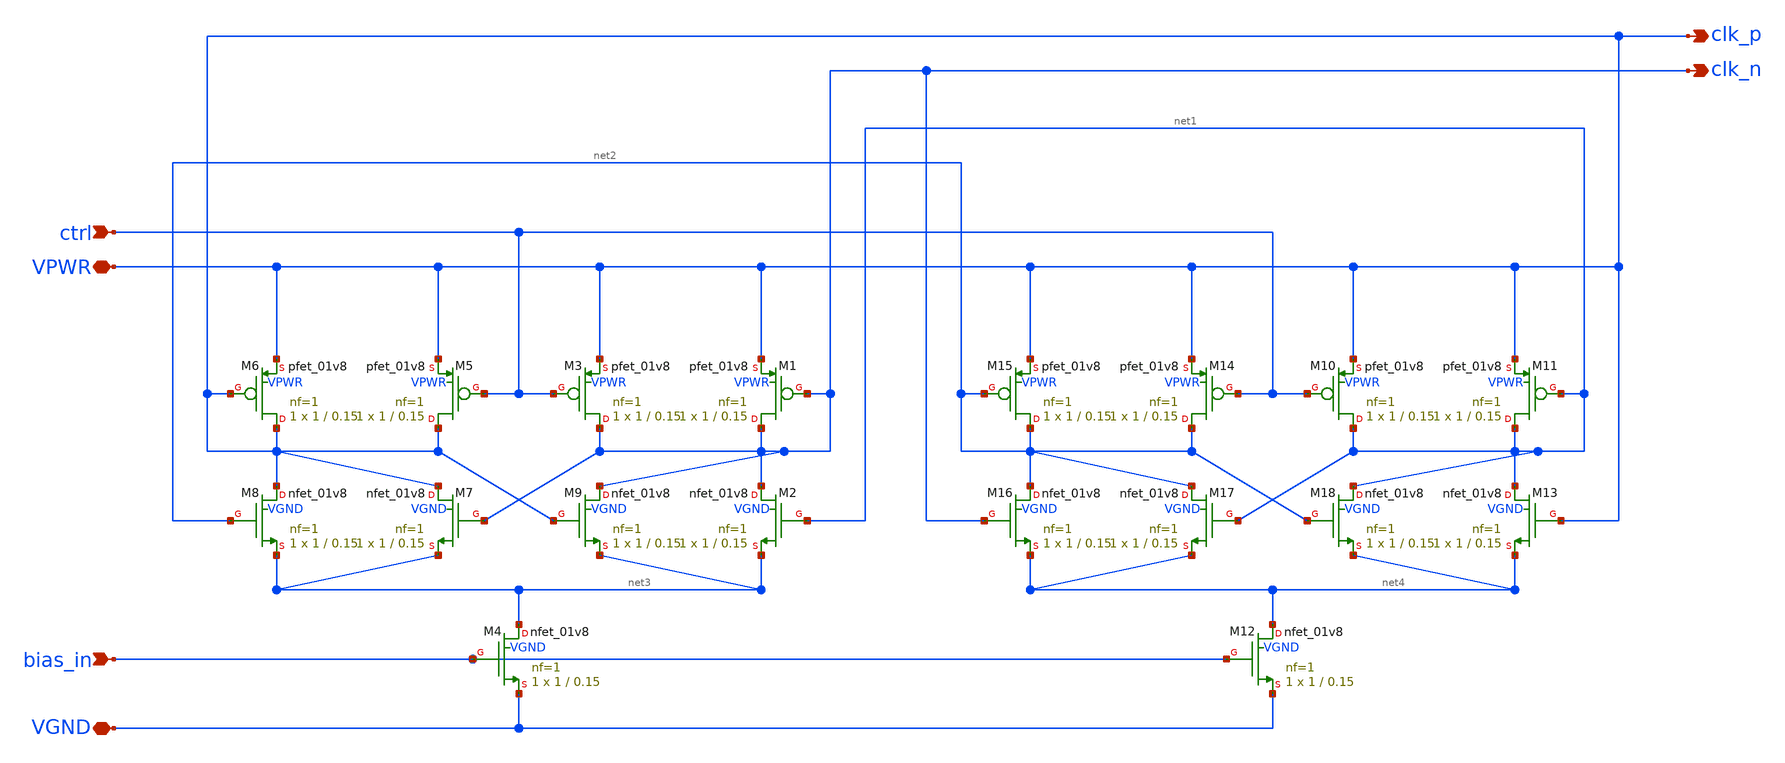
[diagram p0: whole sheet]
** sch_path: simple_vco/v1/clk_core.sch
**.subckt clk_core VPWR VGND ctrl bias_in clk_p clk_n
*.iopin VPWR
*.iopin VGND
*.ipin ctrl
*.ipin bias_in
*.opin clk_p
*.opin clk_n
XM3 clk_n ctrl VPWR VPWR sky130_fd_pr__pfet_01v8 L=0.15 W=1 nf=1 ad='int((1 + 1)/2) * 1 / 1 * 0.29' as='int((1 + 2)/2) * 1 / 1 * 0.29'
+ pd='2*int((1 + 1)/2) * (1 / 1 + 0.29)' ps='2*int((1 + 2)/2) * (1 / 1 + 0.29)' nrd='0.29 / 1 ' nrs='0.29 / 1 '
+ sa=0 sb=0 sd=0 mult=1 m=1
XM1 clk_n clk_n VPWR VPWR sky130_fd_pr__pfet_01v8 L=0.15 W=1 nf=1 ad='int((1 + 1)/2) * 1 / 1 * 0.29'
+ as='int((1 + 2)/2) * 1 / 1 * 0.29' pd='2*int((1 + 1)/2) * (1 / 1 + 0.29)' ps='2*int((1 + 2)/2) * (1 / 1 + 0.29)'
+ nrd='0.29 / 1 ' nrs='0.29 / 1 ' sa=0 sb=0 sd=0 mult=1 m=1
XM4 net3 bias_in VGND VGND sky130_fd_pr__nfet_01v8 L=0.15 W=1 nf=1 ad='int((1 + 1)/2) * 1 / 1 * 0.29'
+ as='int((1 + 2)/2) * 1 / 1 * 0.29' pd='2*int((1 + 1)/2) * (1 / 1 + 0.29)' ps='2*int((1 + 2)/2) * (1 / 1 + 0.29)'
+ nrd='0.29 / 1 ' nrs='0.29 / 1 ' sa=0 sb=0 sd=0 mult=1 m=1
XM2 clk_n net1 net3 VGND sky130_fd_pr__nfet_01v8 L=0.15 W=1 nf=1 ad='int((1 + 1)/2) * 1 / 1 * 0.29' as='int((1 + 2)/2) * 1 / 1 * 0.29'
+ pd='2*int((1 + 1)/2) * (1 / 1 + 0.29)' ps='2*int((1 + 2)/2) * (1 / 1 + 0.29)' nrd='0.29 / 1 ' nrs='0.29 / 1 '
+ sa=0 sb=0 sd=0 mult=1 m=1
XM5 VPWR ctrl VPWR VPWR sky130_fd_pr__pfet_01v8 L=0.15 W=1 nf=1 ad='int((1 + 1)/2) * 1 / 1 * 0.29' as='int((1 + 2)/2) * 1 / 1 * 0.29'
+ pd='2*int((1 + 1)/2) * (1 / 1 + 0.29)' ps='2*int((1 + 2)/2) * (1 / 1 + 0.29)' nrd='0.29 / 1 ' nrs='0.29 / 1 '
+ sa=0 sb=0 sd=0 mult=1 m=1
XM6 VPWR VPWR VPWR VPWR sky130_fd_pr__pfet_01v8 L=0.15 W=1 nf=1 ad='int((1 + 1)/2) * 1 / 1 * 0.29' as='int((1 + 2)/2) * 1 / 1 * 0.29'
+ pd='2*int((1 + 1)/2) * (1 / 1 + 0.29)' ps='2*int((1 + 2)/2) * (1 / 1 + 0.29)' nrd='0.29 / 1 ' nrs='0.29 / 1 '
+ sa=0 sb=0 sd=0 mult=1 m=1
XM8 VPWR net2 net3 VGND sky130_fd_pr__nfet_01v8 L=0.15 W=1 nf=1 ad='int((1 + 1)/2) * 1 / 1 * 0.29' as='int((1 + 2)/2) * 1 / 1 * 0.29'
+ pd='2*int((1 + 1)/2) * (1 / 1 + 0.29)' ps='2*int((1 + 2)/2) * (1 / 1 + 0.29)' nrd='0.29 / 1 ' nrs='0.29 / 1 '
+ sa=0 sb=0 sd=0 mult=1 m=1
XM7 VPWR clk_n net3 VGND sky130_fd_pr__nfet_01v8 L=0.15 W=1 nf=1 ad='int((1 + 1)/2) * 1 / 1 * 0.29' as='int((1 + 2)/2) * 1 / 1 * 0.29'
+ pd='2*int((1 + 1)/2) * (1 / 1 + 0.29)' ps='2*int((1 + 2)/2) * (1 / 1 + 0.29)' nrd='0.29 / 1 ' nrs='0.29 / 1 '
+ sa=0 sb=0 sd=0 mult=1 m=1
XM9 clk_n VPWR net3 VGND sky130_fd_pr__nfet_01v8 L=0.15 W=1 nf=1 ad='int((1 + 1)/2) * 1 / 1 * 0.29' as='int((1 + 2)/2) * 1 / 1 * 0.29'
+ pd='2*int((1 + 1)/2) * (1 / 1 + 0.29)' ps='2*int((1 + 2)/2) * (1 / 1 + 0.29)' nrd='0.29 / 1 ' nrs='0.29 / 1 '
+ sa=0 sb=0 sd=0 mult=1 m=1
XM10 net1 ctrl VPWR VPWR sky130_fd_pr__pfet_01v8 L=0.15 W=1 nf=1 ad='int((1 + 1)/2) * 1 / 1 * 0.29' as='int((1 + 2)/2) * 1 / 1 * 0.29'
+ pd='2*int((1 + 1)/2) * (1 / 1 + 0.29)' ps='2*int((1 + 2)/2) * (1 / 1 + 0.29)' nrd='0.29 / 1 ' nrs='0.29 / 1 '
+ sa=0 sb=0 sd=0 mult=1 m=1
XM11 net1 net1 VPWR VPWR sky130_fd_pr__pfet_01v8 L=0.15 W=1 nf=1 ad='int((1 + 1)/2) * 1 / 1 * 0.29' as='int((1 + 2)/2) * 1 / 1 * 0.29'
+ pd='2*int((1 + 1)/2) * (1 / 1 + 0.29)' ps='2*int((1 + 2)/2) * (1 / 1 + 0.29)' nrd='0.29 / 1 ' nrs='0.29 / 1 '
+ sa=0 sb=0 sd=0 mult=1 m=1
XM12 net4 bias_in VGND VGND sky130_fd_pr__nfet_01v8 L=0.15 W=1 nf=1 ad='int((1 + 1)/2) * 1 / 1 * 0.29'
+ as='int((1 + 2)/2) * 1 / 1 * 0.29' pd='2*int((1 + 1)/2) * (1 / 1 + 0.29)' ps='2*int((1 + 2)/2) * (1 / 1 + 0.29)'
+ nrd='0.29 / 1 ' nrs='0.29 / 1 ' sa=0 sb=0 sd=0 mult=1 m=1
XM13 net1 VPWR net4 VGND sky130_fd_pr__nfet_01v8 L=0.15 W=1 nf=1 ad='int((1 + 1)/2) * 1 / 1 * 0.29' as='int((1 + 2)/2) * 1 / 1 * 0.29'
+ pd='2*int((1 + 1)/2) * (1 / 1 + 0.29)' ps='2*int((1 + 2)/2) * (1 / 1 + 0.29)' nrd='0.29 / 1 ' nrs='0.29 / 1 '
+ sa=0 sb=0 sd=0 mult=1 m=1
XM14 net2 ctrl VPWR VPWR sky130_fd_pr__pfet_01v8 L=0.15 W=1 nf=1 ad='int((1 + 1)/2) * 1 / 1 * 0.29' as='int((1 + 2)/2) * 1 / 1 * 0.29'
+ pd='2*int((1 + 1)/2) * (1 / 1 + 0.29)' ps='2*int((1 + 2)/2) * (1 / 1 + 0.29)' nrd='0.29 / 1 ' nrs='0.29 / 1 '
+ sa=0 sb=0 sd=0 mult=1 m=1
XM15 net2 net2 VPWR VPWR sky130_fd_pr__pfet_01v8 L=0.15 W=1 nf=1 ad='int((1 + 1)/2) * 1 / 1 * 0.29' as='int((1 + 2)/2) * 1 / 1 * 0.29'
+ pd='2*int((1 + 1)/2) * (1 / 1 + 0.29)' ps='2*int((1 + 2)/2) * (1 / 1 + 0.29)' nrd='0.29 / 1 ' nrs='0.29 / 1 '
+ sa=0 sb=0 sd=0 mult=1 m=1
XM16 net2 clk_n net4 VGND sky130_fd_pr__nfet_01v8 L=0.15 W=1 nf=1 ad='int((1 + 1)/2) * 1 / 1 * 0.29'
+ as='int((1 + 2)/2) * 1 / 1 * 0.29' pd='2*int((1 + 1)/2) * (1 / 1 + 0.29)' ps='2*int((1 + 2)/2) * (1 / 1 + 0.29)'
+ nrd='0.29 / 1 ' nrs='0.29 / 1 ' sa=0 sb=0 sd=0 mult=1 m=1
XM17 net2 net1 net4 VGND sky130_fd_pr__nfet_01v8 L=0.15 W=1 nf=1 ad='int((1 + 1)/2) * 1 / 1 * 0.29' as='int((1 + 2)/2) * 1 / 1 * 0.29'
+ pd='2*int((1 + 1)/2) * (1 / 1 + 0.29)' ps='2*int((1 + 2)/2) * (1 / 1 + 0.29)' nrd='0.29 / 1 ' nrs='0.29 / 1 '
+ sa=0 sb=0 sd=0 mult=1 m=1
XM18 net1 net2 net4 VGND sky130_fd_pr__nfet_01v8 L=0.15 W=1 nf=1 ad='int((1 + 1)/2) * 1 / 1 * 0.29' as='int((1 + 2)/2) * 1 / 1 * 0.29'
+ pd='2*int((1 + 1)/2) * (1 / 1 + 0.29)' ps='2*int((1 + 2)/2) * (1 / 1 + 0.29)' nrd='0.29 / 1 ' nrs='0.29 / 1 '
+ sa=0 sb=0 sd=0 mult=1 m=1
**.ends
.end
